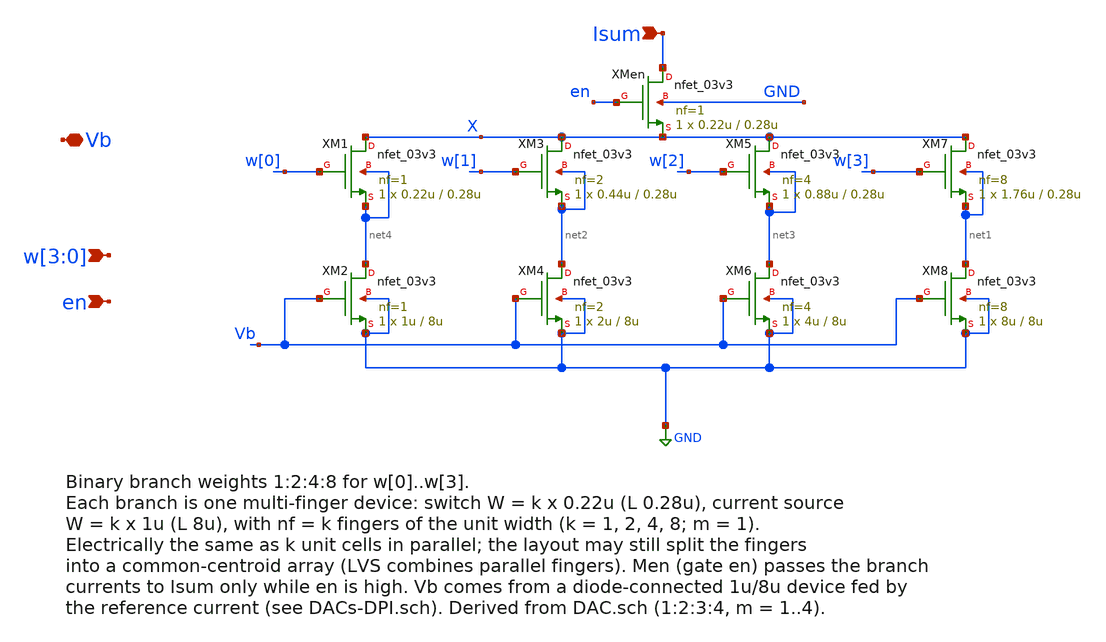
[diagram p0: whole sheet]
** sch_path: analog/neuron/DAC_binary.sch
**.subckt DAC_binary Vb w[3],w[2],w[1],w[0] Isum en
*.iopin Vb
*.ipin w[3],w[2],w[1],w[0]
*.ipin Isum
*.ipin en
XM1 X w[0] net4 net4 nfet_03v3 L=0.28u W=0.22u nf=1 ad='int((nf+1)/2) * W/nf * 0.18u' as='int((nf+2)/2) * W/nf * 0.18u'
+ pd='2*int((nf+1)/2) * (W/nf + 0.18u)' ps='2*int((nf+2)/2) * (W/nf + 0.18u)' nrd='0.18u / W' nrs='0.18u / W'
+ sa=0 sb=0 sd=0 m=1
XM2 net4 Vb GND GND nfet_03v3 L=8u W=1u nf=1 ad='int((nf+1)/2) * W/nf * 0.18u' as='int((nf+2)/2) * W/nf * 0.18u'
+ pd='2*int((nf+1)/2) * (W/nf + 0.18u)' ps='2*int((nf+2)/2) * (W/nf + 0.18u)' nrd='0.18u / W' nrs='0.18u / W'
+ sa=0 sb=0 sd=0 m=1
XM3 X w[1] net2 net2 nfet_03v3 L=0.28u W=0.44u nf=2 ad='int((nf+1)/2) * W/nf * 0.18u' as='int((nf+2)/2) * W/nf * 0.18u'
+ pd='2*int((nf+1)/2) * (W/nf + 0.18u)' ps='2*int((nf+2)/2) * (W/nf + 0.18u)' nrd='0.18u / W' nrs='0.18u / W'
+ sa=0 sb=0 sd=0 m=1
XM4 net2 Vb GND GND nfet_03v3 L=8u W=2u nf=2 ad='int((nf+1)/2) * W/nf * 0.18u' as='int((nf+2)/2) * W/nf * 0.18u'
+ pd='2*int((nf+1)/2) * (W/nf + 0.18u)' ps='2*int((nf+2)/2) * (W/nf + 0.18u)' nrd='0.18u / W' nrs='0.18u / W'
+ sa=0 sb=0 sd=0 m=1
XM5 X w[2] net3 net3 nfet_03v3 L=0.28u W=0.88u nf=4 ad='int((nf+1)/2) * W/nf * 0.18u' as='int((nf+2)/2) * W/nf * 0.18u'
+ pd='2*int((nf+1)/2) * (W/nf + 0.18u)' ps='2*int((nf+2)/2) * (W/nf + 0.18u)' nrd='0.18u / W' nrs='0.18u / W'
+ sa=0 sb=0 sd=0 m=1
XM6 net3 Vb GND GND nfet_03v3 L=8u W=4u nf=4 ad='int((nf+1)/2) * W/nf * 0.18u' as='int((nf+2)/2) * W/nf * 0.18u'
+ pd='2*int((nf+1)/2) * (W/nf + 0.18u)' ps='2*int((nf+2)/2) * (W/nf + 0.18u)' nrd='0.18u / W' nrs='0.18u / W'
+ sa=0 sb=0 sd=0 m=1
XM7 X w[3] net1 net1 nfet_03v3 L=0.28u W=1.76u nf=8 ad='int((nf+1)/2) * W/nf * 0.18u' as='int((nf+2)/2) * W/nf * 0.18u'
+ pd='2*int((nf+1)/2) * (W/nf + 0.18u)' ps='2*int((nf+2)/2) * (W/nf + 0.18u)' nrd='0.18u / W' nrs='0.18u / W'
+ sa=0 sb=0 sd=0 m=1
XM8 net1 Vb GND GND nfet_03v3 L=8u W=8u nf=8 ad='int((nf+1)/2) * W/nf * 0.18u' as='int((nf+2)/2) * W/nf * 0.18u'
+ pd='2*int((nf+1)/2) * (W/nf + 0.18u)' ps='2*int((nf+2)/2) * (W/nf + 0.18u)' nrd='0.18u / W' nrs='0.18u / W'
+ sa=0 sb=0 sd=0 m=1
XMen Isum en X GND nfet_03v3 L=0.28u W=0.22u nf=1 ad='int((nf+1)/2) * W/nf * 0.18u' as='int((nf+2)/2) * W/nf * 0.18u'
+ pd='2*int((nf+1)/2) * (W/nf + 0.18u)' ps='2*int((nf+2)/2) * (W/nf + 0.18u)' nrd='0.18u / W' nrs='0.18u / W'
+ sa=0 sb=0 sd=0 m=1
**.ends
.GLOBAL GND
.end
